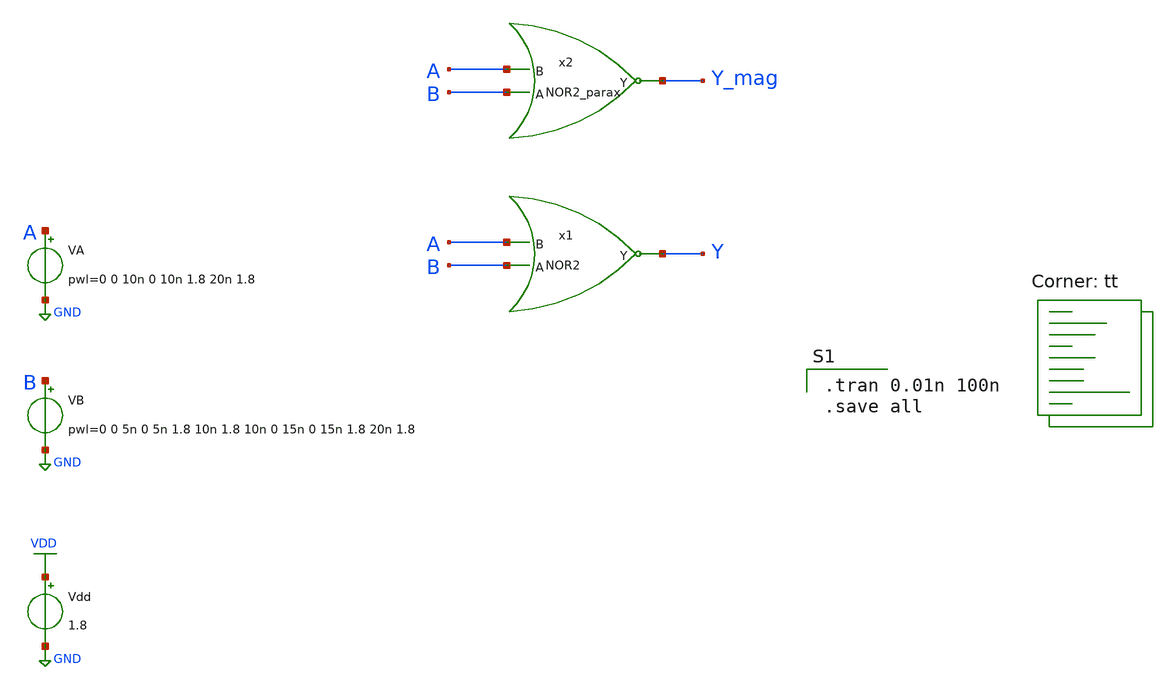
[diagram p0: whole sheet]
** sch_path: nor2sim.sch
**.subckt nor2sim
Vdd VDD GND 1.8
VA A GND pwl=0 0 10n 0 10n 1.8 20n 1.8
VB B GND pwl=0 0 5n 0 5n 1.8 10n 1.8 10n 0 15n 0 15n 1.8 20n 1.8
x1 A Y B NOR2
x2 A Y_mag B NOR2_parax
**** begin user architecture code

.tran 0.01n 100n
.save all

.lib $::SKYWATER_MODELS/sky130.lib.spice tt
**** end user architecture code
**.ends

* expanding   symbol:  gates/NOR2.sym # of pins=3
** sym_path: gates/NOR2.sym
** sch_path: gates/NOR2.sch
.subckt NOR2 B Y A
*.ipin A
*.ipin B
*.opin Y
XM7 VDD B net1 VDD sky130_fd_pr__pfet_01v8 L=0.15 W=1 nf=1 ad='int((nf+1)/2) * W/nf * 0.29' as='int((nf+2)/2) * W/nf * 0.29'
+ pd='2*int((nf+1)/2) * (W/nf + 0.29)' ps='2*int((nf+2)/2) * (W/nf + 0.29)' nrd='0.29 / W' nrs='0.29 / W'
+ sa=0 sb=0 sd=0 mult=1 m=1
XM8 GND B Y GND sky130_fd_pr__nfet_01v8 L=0.15 W=1 nf=1 ad='int((nf+1)/2) * W/nf * 0.29' as='int((nf+2)/2) * W/nf * 0.29'
+ pd='2*int((nf+1)/2) * (W/nf + 0.29)' ps='2*int((nf+2)/2) * (W/nf + 0.29)' nrd='0.29 / W' nrs='0.29 / W'
+ sa=0 sb=0 sd=0 mult=1 m=1
XM9 net1 A Y VDD sky130_fd_pr__pfet_01v8 L=0.15 W=1 nf=1 ad='int((nf+1)/2) * W/nf * 0.29' as='int((nf+2)/2) * W/nf * 0.29'
+ pd='2*int((nf+1)/2) * (W/nf + 0.29)' ps='2*int((nf+2)/2) * (W/nf + 0.29)' nrd='0.29 / W' nrs='0.29 / W'
+ sa=0 sb=0 sd=0 mult=1 m=1
XM10 GND A Y GND sky130_fd_pr__nfet_01v8 L=0.15 W=1 nf=1 ad='int((nf+1)/2) * W/nf * 0.29' as='int((nf+2)/2) * W/nf * 0.29'
+ pd='2*int((nf+1)/2) * (W/nf + 0.29)' ps='2*int((nf+2)/2) * (W/nf + 0.29)' nrd='0.29 / W' nrs='0.29 / W'
+ sa=0 sb=0 sd=0 mult=1 m=1
.ends


* expanding   symbol:  gates/NOR2_parax.sym # of pins=3
** sym_path: gates/NOR2.sym
.include [file normalize /home/apn/mag_gates/NOR2_parax.spice]
.GLOBAL VDD
.GLOBAL GND
.end
